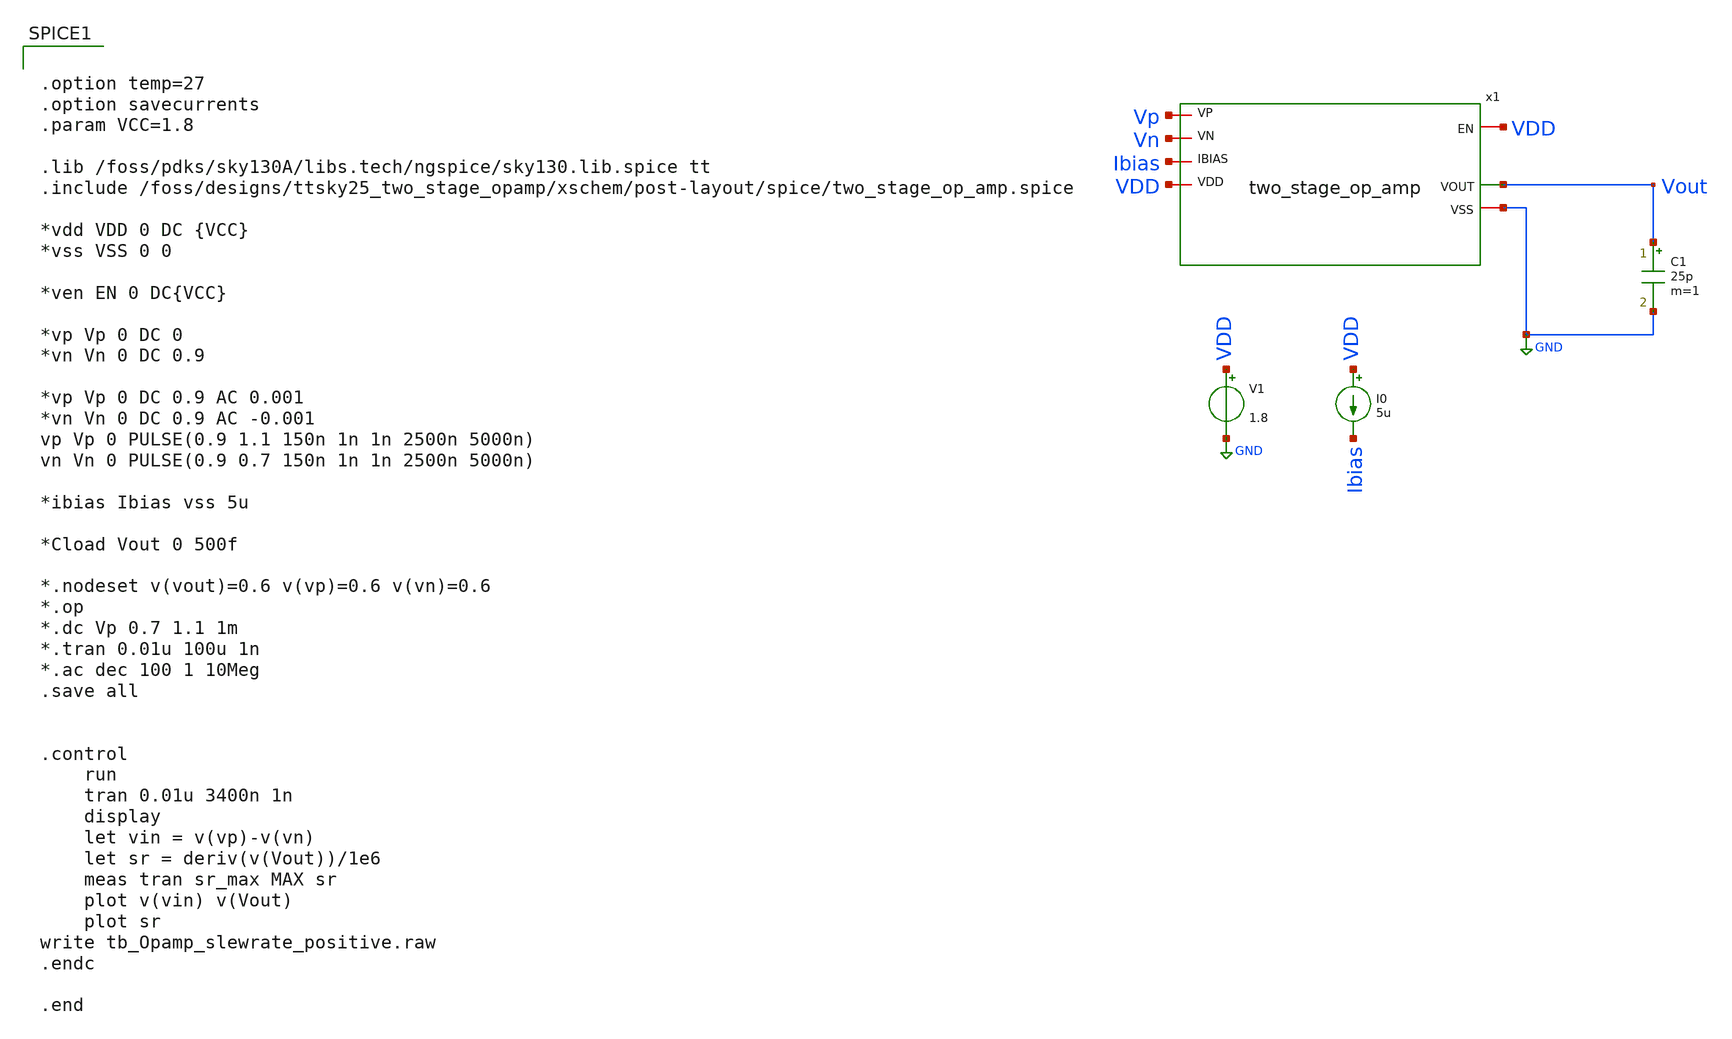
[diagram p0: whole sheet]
** sch_path: xschem/post-layout/testbenches/tb_Opamp_slewrate_positive.sch
**.subckt tb_Opamp_slewrate_positive
V1 VDD GND 1.8
I0 VDD Ibias 5u
C1 Vout GND 25p m=1
x1 VDD GND Ibias Vout Vp Vn VDD two_stage_op_amp
**** begin user architecture code


.option temp=27
.option savecurrents
.param VCC=1.8

.lib /foss/pdks/sky130A/libs.tech/ngspice/sky130.lib.spice tt
.include /foss/designs/ttsky25_two_stage_opamp/xschem/post-layout/spice/two_stage_op_amp.spice

*vdd VDD 0 DC {VCC}
*vss VSS 0 0

*ven EN 0 DC{VCC}

*vp Vp 0 DC 0
*vn Vn 0 DC 0.9

*vp Vp 0 DC 0.9 AC 0.001
*vn Vn 0 DC 0.9 AC -0.001
vp Vp 0 PULSE(0.9 1.1 150n 1n 1n 2500n 5000n)
vn Vn 0 PULSE(0.9 0.7 150n 1n 1n 2500n 5000n)

*ibias Ibias vss 5u

*Cload Vout 0 500f

*.nodeset v(vout)=0.6 v(vp)=0.6 v(vn)=0.6
*.op
*.dc Vp 0.7 1.1 1m
*.tran 0.01u 100u 1n
*.ac dec 100 1 10Meg
.save all


.control
	run
	tran 0.01u 3400n 1n
	display
	let vin = v(vp)-v(vn)
	let sr = deriv(v(Vout))/1e6
	meas tran sr_max MAX sr
	plot v(vin) v(Vout)
	plot sr
write tb_Opamp_slewrate_positive.raw
.endc

.end


**** end user architecture code
**.ends
.GLOBAL GND
.end
